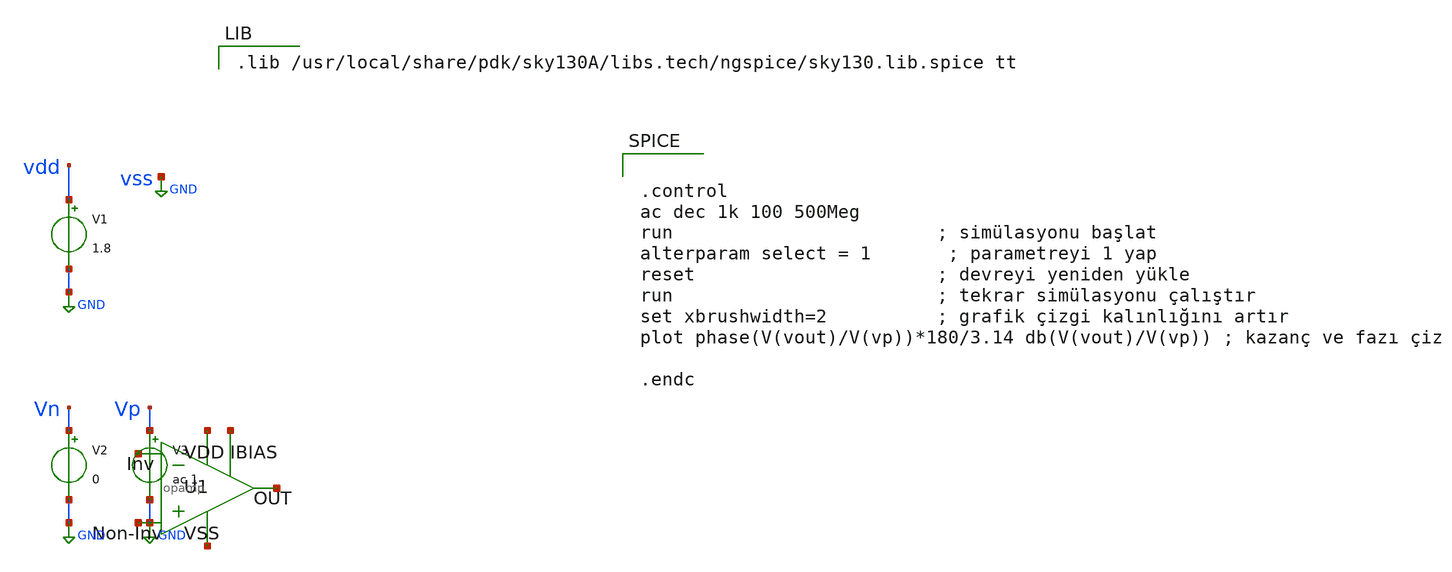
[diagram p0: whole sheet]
** sch_path: ANALOG_FOPID_XSCHEM/OPAMP/opamp_tb.sch
**.subckt opamp_tb
U1 net1 net2 net3 net4 net5 net6 opamp
V1 vdd GND 1.8
V2 Vn GND 0
V3 Vp GND ac 1
**** begin user architecture code


.control
ac dec 1k 100 500Meg
run                        ; simülasyonu başlat
alterparam select = 1       ; parametreyi 1 yap
reset                      ; devreyi yeniden yükle
run                        ; tekrar simülasyonu çalıştır
set xbrushwidth=2          ; grafik çizgi kalınlığını artır
plot phase(V(vout)/V(vp))*180/3.14 db(V(vout)/V(vp)) ; kazanç ve fazı çiz

.endc



.lib /usr/local/share/pdk/sky130A/libs.tech/ngspice/sky130.lib.spice tt

**** end user architecture code
**.ends
.GLOBAL GND
.end
